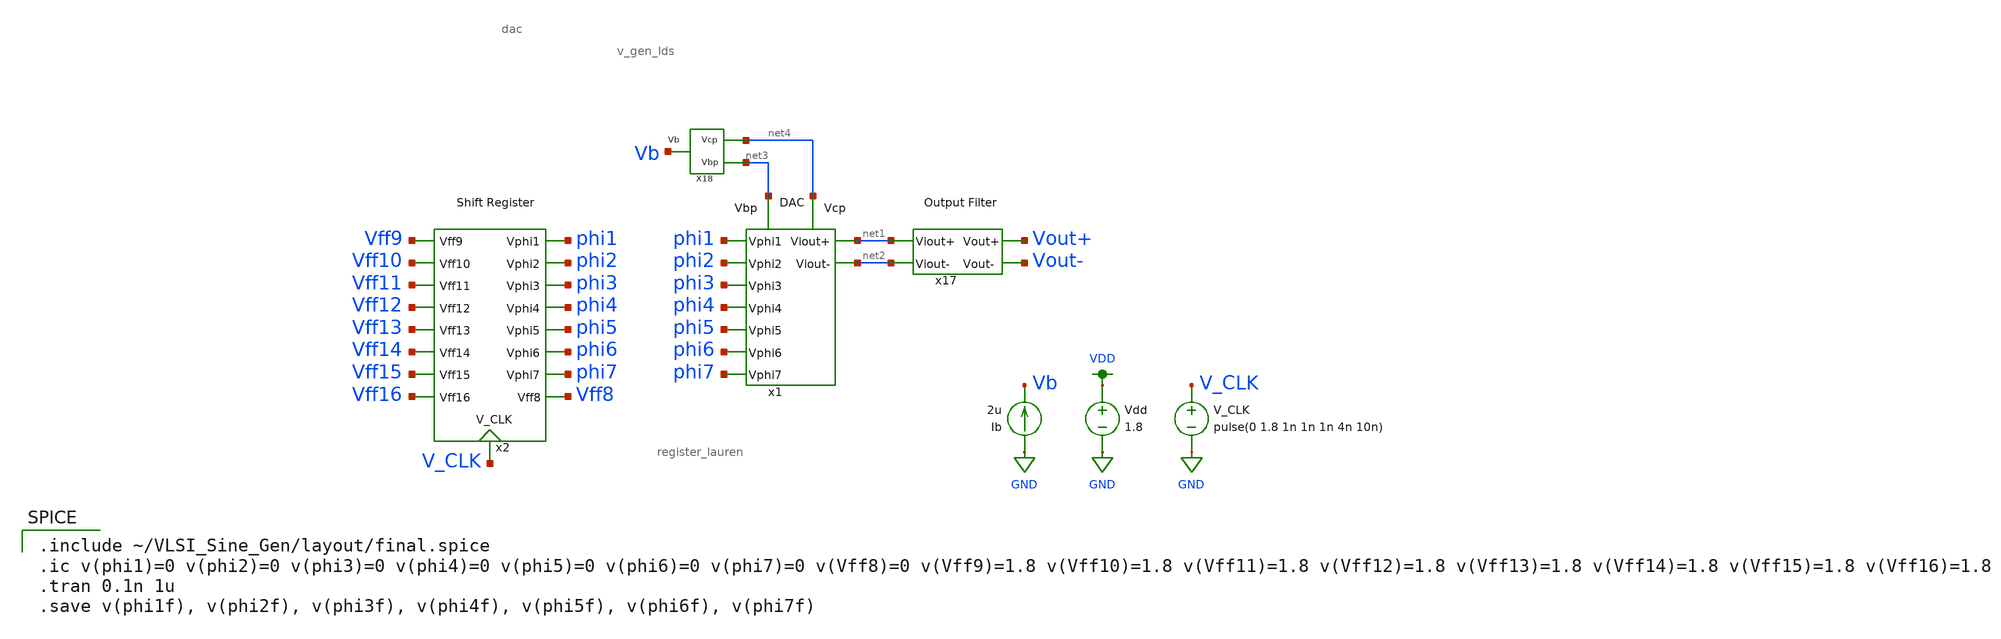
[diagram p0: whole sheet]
** sch_path: simulation/post_layout_sim/register_dac_tran_lauren.sch
**.subckt register_dac_tran_lauren
V_CLK V_CLK GND pulse(0 1.8 1n 1n 1n 4n 10n)
Vdd VDD GND 1.8
x1 phi1 phi2 phi3 phi4 phi5 phi6 phi7 net1 net2 net3 net4 dac
x2 Vff10 Vff11 Vff12 Vff13 Vff14 Vff16 Vff15 Vff9 phi1 phi2 phi3 phi4 phi5 phi6 phi7 Vff8 V_CLK
+ register_lauren
Ib GND Vb 2u
X18 net4 net3 Vb v_gen_lds
x17 net1 net2 Vout+ Vout- filter_lvs
**** begin user architecture code

.option wnflag=1
.param MC_SWITCH=0.0
.lib ~/skywater/skywater-pdk/libraries/sky130_fd_pr_ngspice/latest/models/sky130.lib.spice tt


.include ~/VLSI_Sine_Gen/layout/final.spice
.ic v(phi1)=0 v(phi2)=0 v(phi3)=0 v(phi4)=0 v(phi5)=0 v(phi6)=0 v(phi7)=0 v(Vff8)=0 v(Vff9)=1.8
+ v(Vff10)=1.8 v(Vff11)=1.8 v(Vff12)=1.8 v(Vff13)=1.8 v(Vff14)=1.8 v(Vff15)=1.8 v(Vff16)=1.8
.tran 0.1n 1u
.save v(phi1f), v(phi2f), v(phi3f), v(phi4f), v(phi5f), v(phi6f), v(phi7f)

**** end user architecture code
**.ends
.GLOBAL GND
.GLOBAL VDD
.end
